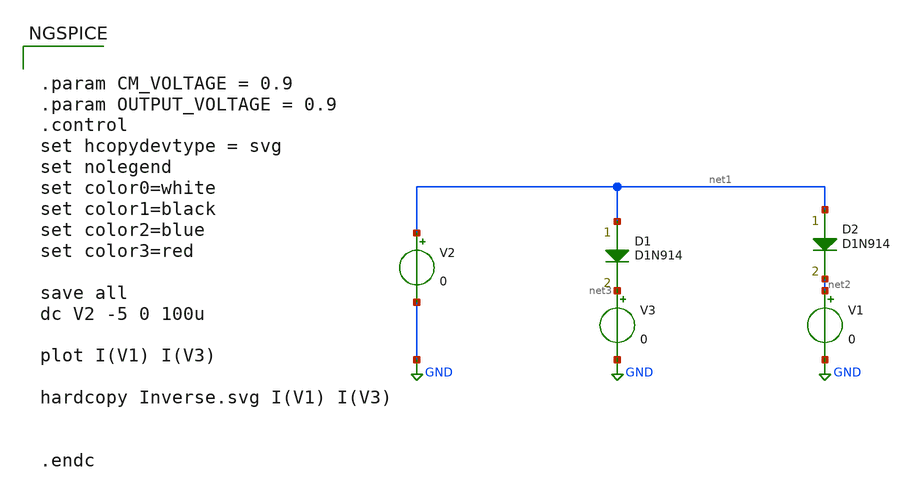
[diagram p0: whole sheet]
** sch_path: analog/xschem/Diode_Dtemp_tb.sch
**.subckt Diode_Dtemp_tb
V2 net1 GND 0
V1 net2 GND 0
V3 net3 GND 0
D1 net1 net3 D1N914 area=1
D2 net1 net2 D1N914 area=1
**** begin user architecture code


.param CM_VOLTAGE = 0.9
.param OUTPUT_VOLTAGE = 0.9
.control
set hcopydevtype = svg
set nolegend
set color0=white
set color1=black
set color2=blue
set color3=red

save all
dc V2 -5 0 100u

plot I(V1) I(V3)

hardcopy Inverse.svg I(V1) I(V3)


.endc



*.lib $::SKYWATER_MODELS/models/sky130.lib.spice tt
.lib /home/icarosix/asic/pdks/sky130A/libs.tech/ngspice/sky130.lib.spice tt
.option wnflag=1

**** end user architecture code
**.ends
.GLOBAL GND
**** begin user architecture code
[sky130_models]
**** end user architecture code
.end
